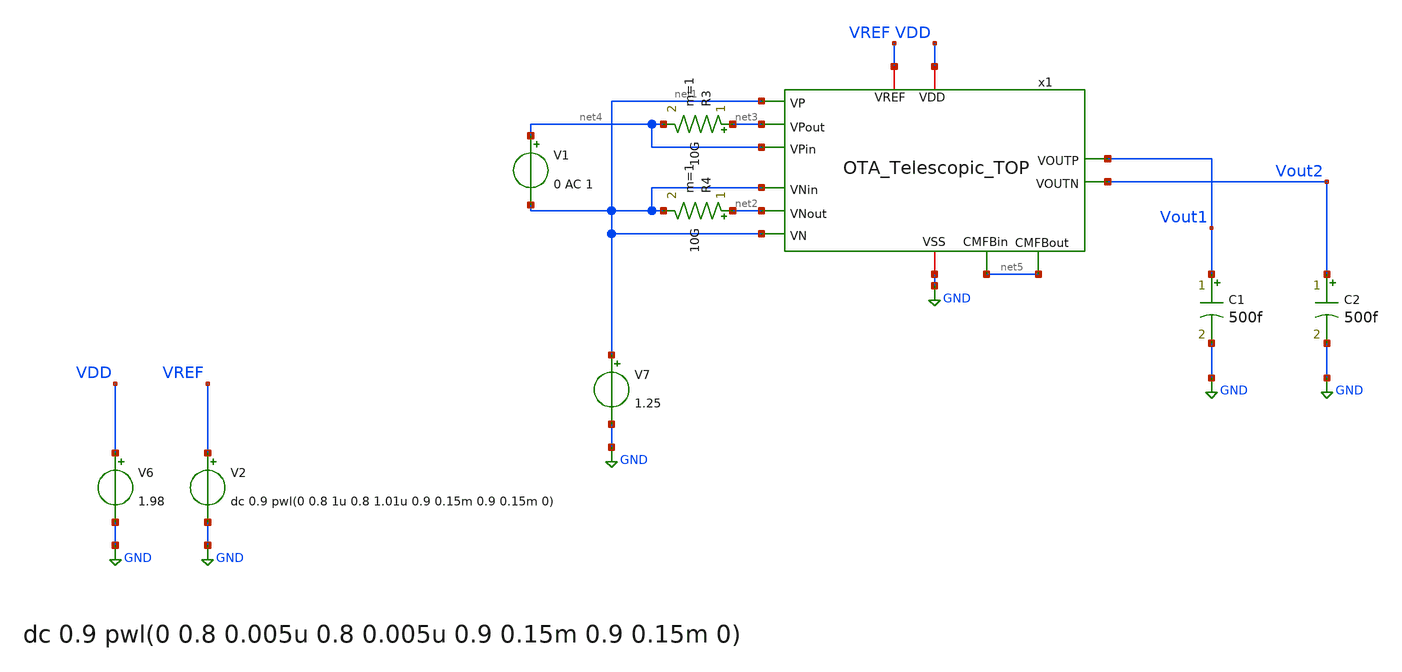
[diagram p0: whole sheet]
** sch_path: OTA_Telescopic/OTA_Telescopic_TOP_TB_OL.sch
**.subckt OTA_Telescopic_TOP_TB_OL
V7 net1 GND 1.25
C1 Vout1 GND 500f m=1
C2 Vout2 GND 500f m=1
x1 VDD GND net3 net1 net4 Vout2 Vout1 net1 net2 net1 VREF net5 net5 OTA_Telescopic_TOP
V6 VDD GND 1.98
R3 net3 net4 10G m=1
R4 net2 net1 10G m=1
V1 net4 net1 0 AC 1
V2 VREF GND dc 0.9 pwl(0 0.8 1u 0.8 1.01u 0.9 0.15m 0.9 0.15m 0)
**** begin user architecture code

** opencircuitdesign pdks install
.lib cornerMOSlv.lib mos_ff
.lib cornerRES.lib res_typ
.lib cornerCAP.lib cap_typ
.temp 0



.control
save all
 set color0 = white

* AC simulation
ac dec 1k 1 1T
let Av = db((v(Vout2)-v(Vout1)))
meas ac Ao FIND Av WHEN frequency=10
let ABW = Ao-3
meas ac BW WHEN Av=ABW
meas ac UGBW WHEN Av=0
let phase_vec = 180/pi*cph(v(Vout2)-v(Vout1))

* Phase margin (PM)
meas ac phase FIND phase_vec WHEN frequency=UGBW
let PM = phase+180
print PM

* Gain margin (GM)
meas ac freq180 FIND frequency WHEN phase_vec=-180
meas ac gain FIND Av WHEN frequency=freq180
let GM = 0-gain

*BW in 7 dB
meas ac UGBW7dB WHEN Av=7
meas ac UGBW4dB WHEN Av=4

print GM
plot Av
plot phase_vec

plot db(v(x1.Vo1)-v(x1.Vo2))

write AC_OL.raw

wrdata AvOL_ Av
wrdata PhaseOL_ phase_vec


*DC simulation

op
let vout_dc = v(Vout1)
print vout_dc
write OTA_Telescopic_TOP_TB_OL.raw


reset
noise v(Vout1) V6 dec 100 1 0.5e9 1
setplot noise1
*plot onoise_spectrum
setplot noise2
print onoise_total

.endc




.op

.save all

.save @n.x1.xm3.nsg13_lv_pmos[ids]
.save @n.x1.xm3.nsg13_lv_pmos[gm]

.save @n.x1.xm2.nsg13_lv_nmos[ids]
.save @n.x1.xm2.nsg13_lv_nmos[gm]

*OTA
.save @n.x1.x1.xm1.nsg13_lv_nmos[ids]
.save @n.x1.x1.xm1.nsg13_lv_nmos[gm]
.save @n.x1.x1.xm2.nsg13_lv_nmos[ids]
.save @n.x1.x1.xm2.nsg13_lv_nmos[gm]

.save @n.x1.x1.xm9.nsg13_lv_pmos[ids]
.save @n.x1.x1.xm9.nsg13_lv_pmos[gm]
.save @n.x1.x1.xm10.nsg13_lv_pmos[ids]
.save @n.x1.x1.xm10.nsg13_lv_pmos[gm]

.save @n.x1.x1.xm0.nsg13_lv_nmos[ids]

.save @n.x1.x1.xm1.nsg13_lv_nmos[vsat]

.save @n.x1.x1.xm7.nsg13_lv_pmos[ids]
.save @n.x1.x1.xm7.nsg13_lv_pmos[gm]
.save @n.x1.x1.xm1.nsg13_lv_pmos[vdss]

.save @n.x1.x1.xm13.nsg13_lv_nmos[ids]
.save @n.x1.x1.xm14.nsg13_lv_nmos[ids]
.save @n.x1.x1.xm15.nsg13_lv_nmos[ids]
.save @n.x1.x1.xm16.nsg13_lv_nmos[ids]
.save @n.x1.x1.xm17.nsg13_lv_nmos[ids]

.save @n.x1.x1.xm18.nsg13_lv_pmos[ids]
.save @n.x1.x1.xm19.nsg13_lv_pmos[ids]

*CMFB
.save @n.x1.x2.xm0.nsg13_lv_pmos[ids]
.save @n.x1.x2.xm1.nsg13_lv_pmos[ids]
.save @n.x1.x2.xm1.nsg13_lv_pmos[gm]
.save @n.x1.x2.xm2.nsg13_lv_pmos[ids]
.save @n.x1.x2.xm2.nsg13_lv_pmos[gm]
.save @n.x1.x2.xm3.nsg13_lv_pmos[ids]
.save @n.x1.x2.xm3.nsg13_lv_pmos[gm]
.save @n.x1.x2.xm4.nsg13_lv_pmos[ids]
.save @n.x1.x2.xm4.nsg13_lv_pmos[gm]
.save @n.x1.x2.xm5.nsg13_lv_pmos[ids]
.save @n.x1.x2.xm5.nsg13_lv_pmos[gm]
.save @n.x1.x2.xm6.nsg13_lv_pmos[ids]
.save @n.x1.x2.xm6.nsg13_lv_pmos[gm]

.save @n.x1.x2.xm7.nsg13_lv_nmos[ids]
.save @n.x1.x2.xm7.nsg13_lv_nmos[gm]
.save @n.x1.x2.xm8.nsg13_lv_nmos[ids]
.save @n.x1.x2.xm8.nsg13_lv_nmos[gm]



.control

let vsat_M1 = @n.x1.x1.xm1.nsg13_lv_nmos[vsat]
let vsat_M3 = @n.x1.x1.xm3.nsg13_lv_nmos[vsat]
let vsat_M5 = @n.x1.x1.xm5.nsg13_lv_pmos[vsat]
let vsat_M7 = @n.x1.x1.xm7.nsg13_lv_pmos[vsat]
let vsat_M0 = @n.x1.x1.xm0.nsg13_lv_nmos[vsat]

let vsat_M9 = @n.x1.x1.xm9.nsg13_lv_pmos[vsat]
let vsat_M11 = @n.x1.x1.xm11.nsg13_lv_nmos[vsat]

print vsat_M1
print vsat_M3
print vsat_M5
print vsat_M7
print vsat_M0
print vsat_M9
print vsat_M11

let ro_M1 = 1/@n.x1.x1.xm1.nsg13_lv_nmos[gds]
let ro_M3 = 1/@n.x1.x1.xm3.nsg13_lv_nmos[gds]
let ro_M5 = 1/@n.x1.x1.xm5.nsg13_lv_pmos[gds]
let ro_M7 = 1/@n.x1.x1.xm7.nsg13_lv_pmos[gds]
let ro_M0 = 1/@n.x1.x1.xm0.nsg13_lv_nmos[gds]

print ro_M1
print ro_M3
print ro_M5
print ro_M7
print ro_M0

let gm_M1 = @n.x1.x1.xm1.nsg13_lv_nmos[gm]
let gm_M3 = @n.x1.x1.xm3.nsg13_lv_nmos[gm]
let gm_M5 = @n.x1.x1.xm5.nsg13_lv_pmos[gm]
let gm_M7 = @n.x1.x1.xm7.nsg13_lv_pmos[gm]
let gm_M0 = @n.x1.x1.xm0.nsg13_lv_nmos[gm]

print gm_M1
print gm_M3
print gm_M5
print gm_M7
print gm_M0

let gmb_M3 = @n.x1.x1.xm3.nsg13_lv_nmos[gmb]
let gmb_M5 = @n.x1.x1.xm5.nsg13_lv_pmos[gmb]

print gmb_M3
print gmb_M5


*CMFB

let x2_vsat_M0 = @n.x1.x2.xm0.nsg13_lv_pmos[vsat]
let x2_vth_M0 = @n.x1.x2.xm0.nsg13_lv_pmos[vth]

print x2_vsat_M0
print x2_vth_M0

.endc



**** end user architecture code
**.ends
.GLOBAL GND
.end
